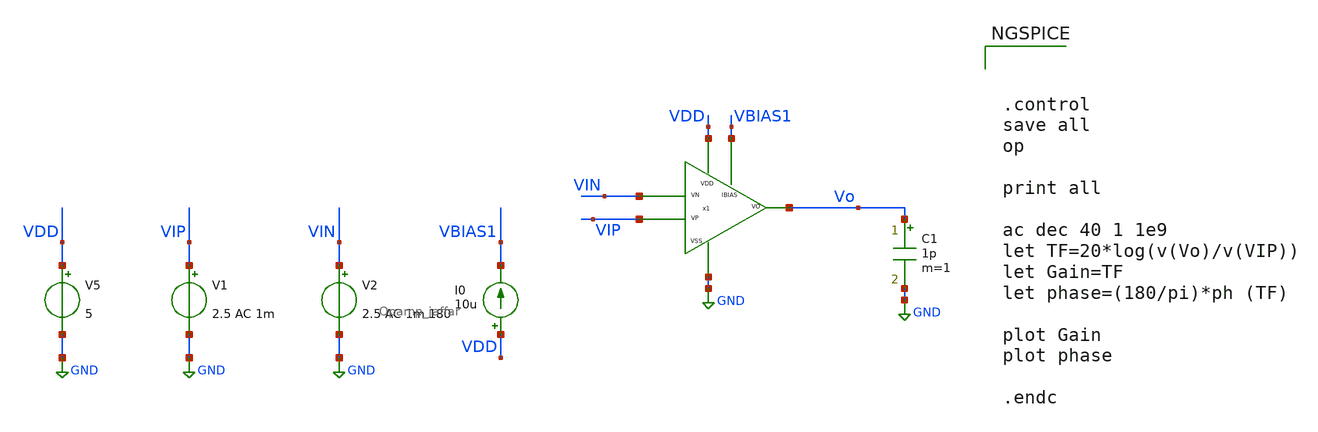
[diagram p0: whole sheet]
** sch_path: xschem/xschem_BGR_Top/Opamp_jaffar_tb_ac.sch
**.subckt Opamp_jaffar_tb_ac
V1 VIP GND 2.5 AC 1m
V2 VIN GND 2.5 AC 1m 180
V5 VDD GND 5
I0 VDD VBIAS1 10u
C1 Vo GND 1p m=1
x1 VDD GND VIP VIN Vo VBIAS1 Opamp_jaffar
**** begin user architecture code



.control
save all
op

print all

ac dec 40 1 1e9
let TF=20*log(v(Vo)/v(VIP))
let Gain=TF
let phase=(180/pi)*ph (TF)

plot Gain
plot phase

.endc


** manual skywater pdks install (with patches applied)
* .lib $::SKYWATER_MODELS/models/sky130.lib.spice tt

** opencircuitdesign pdks install
.lib $::SKYWATER_MODELS/sky130.lib.spice tt


**** end user architecture code
**.ends

* expanding   symbol:  Opamp_jaffar.sym # of pins=6
** sym_path: xschem/xschem_BGR_Top/Opamp_jaffar.sym
** sch_path: xschem/xschem_BGR_Top/Opamp_jaffar.sch
.subckt Opamp_jaffar VDD VSS VP VN VO IBIAS
*.iopin VDD
*.iopin VSS
*.iopin VP
*.iopin VN
*.iopin VO
*.iopin IBIAS
XC1 net7 VO sky130_fd_pr__cap_mim_m3_1 W=24 L=24 MF=1 m=1
XC2 VDD VSS sky130_fd_pr__cap_mim_m3_1 W=30 L=10 MF=1 m=1
XC3 VDD VSS sky130_fd_pr__cap_mim_m3_1 W=30 L=10 MF=1 m=1
XM30 net2 net1 VDD VDD sky130_fd_pr__pfet_g5v0d10v5 L=1 W=5 nf=1 ad='int((nf+1)/2) * W/nf * 0.29' as='int((nf+2)/2) * W/nf * 0.29'
+ pd='2*int((nf+1)/2) * (W/nf + 0.29)' ps='2*int((nf+2)/2) * (W/nf + 0.29)' nrd='0.29 / W' nrs='0.29 / W'
+ sa=0 sb=0 sd=0 mult=1 m=1
XM32 net1 net1 VDD VDD sky130_fd_pr__pfet_g5v0d10v5 L=1 W=5 nf=1 ad='int((nf+1)/2) * W/nf * 0.29' as='int((nf+2)/2) * W/nf * 0.29'
+ pd='2*int((nf+1)/2) * (W/nf + 0.29)' ps='2*int((nf+2)/2) * (W/nf + 0.29)' nrd='0.29 / W' nrs='0.29 / W'
+ sa=0 sb=0 sd=0 mult=1 m=1
XM31 net1 VN net3 VSS sky130_fd_pr__nfet_g5v0d10v5 L=1 W=50 nf=5 ad='int((nf+1)/2) * W/nf * 0.29' as='int((nf+2)/2) * W/nf * 0.29'
+ pd='2*int((nf+1)/2) * (W/nf + 0.29)' ps='2*int((nf+2)/2) * (W/nf + 0.29)' nrd='0.29 / W' nrs='0.29 / W'
+ sa=0 sb=0 sd=0 mult=1 m=1
XM1 net2 VP net3 VSS sky130_fd_pr__nfet_g5v0d10v5 L=1 W=50 nf=5 ad='int((nf+1)/2) * W/nf * 0.29' as='int((nf+2)/2) * W/nf * 0.29'
+ pd='2*int((nf+1)/2) * (W/nf + 0.29)' ps='2*int((nf+2)/2) * (W/nf + 0.29)' nrd='0.29 / W' nrs='0.29 / W'
+ sa=0 sb=0 sd=0 mult=1 m=1
XM2 net3 IBIAS net4 VSS sky130_fd_pr__nfet_g5v0d10v5 L=1 W=50 nf=10 ad='int((nf+1)/2) * W/nf * 0.29'
+ as='int((nf+2)/2) * W/nf * 0.29' pd='2*int((nf+1)/2) * (W/nf + 0.29)' ps='2*int((nf+2)/2) * (W/nf + 0.29)'
+ nrd='0.29 / W' nrs='0.29 / W' sa=0 sb=0 sd=0 mult=1 m=1
XM3 VO IBIAS net6 VSS sky130_fd_pr__nfet_g5v0d10v5 L=1 W=100 nf=20 ad='int((nf+1)/2) * W/nf * 0.29' as='int((nf+2)/2) * W/nf * 0.29'
+ pd='2*int((nf+1)/2) * (W/nf + 0.29)' ps='2*int((nf+2)/2) * (W/nf + 0.29)' nrd='0.29 / W' nrs='0.29 / W'
+ sa=0 sb=0 sd=0 mult=1 m=1
XM4 IBIAS IBIAS net5 VSS sky130_fd_pr__nfet_g5v0d10v5 L=1 W=5 nf=1 ad='int((nf+1)/2) * W/nf * 0.29' as='int((nf+2)/2) * W/nf * 0.29'
+ pd='2*int((nf+1)/2) * (W/nf + 0.29)' ps='2*int((nf+2)/2) * (W/nf + 0.29)' nrd='0.29 / W' nrs='0.29 / W'
+ sa=0 sb=0 sd=0 mult=1 m=1
XM5 net4 net5 VSS VSS sky130_fd_pr__nfet_g5v0d10v5 L=1 W=50 nf=5 ad='int((nf+1)/2) * W/nf * 0.29' as='int((nf+2)/2) * W/nf * 0.29'
+ pd='2*int((nf+1)/2) * (W/nf + 0.29)' ps='2*int((nf+2)/2) * (W/nf + 0.29)' nrd='0.29 / W' nrs='0.29 / W'
+ sa=0 sb=0 sd=0 mult=1 m=1
XM7 net5 net5 VSS VSS sky130_fd_pr__nfet_g5v0d10v5 L=1 W=10 nf=1 ad='int((nf+1)/2) * W/nf * 0.29' as='int((nf+2)/2) * W/nf * 0.29'
+ pd='2*int((nf+1)/2) * (W/nf + 0.29)' ps='2*int((nf+2)/2) * (W/nf + 0.29)' nrd='0.29 / W' nrs='0.29 / W'
+ sa=0 sb=0 sd=0 mult=1 m=1
XM8 net6 net5 VSS VSS sky130_fd_pr__nfet_g5v0d10v5 L=1 W=100 nf=10 ad='int((nf+1)/2) * W/nf * 0.29' as='int((nf+2)/2) * W/nf * 0.29'
+ pd='2*int((nf+1)/2) * (W/nf + 0.29)' ps='2*int((nf+2)/2) * (W/nf + 0.29)' nrd='0.29 / W' nrs='0.29 / W'
+ sa=0 sb=0 sd=0 mult=1 m=1
XM6 VO net2 VDD VDD sky130_fd_pr__pfet_g5v0d10v5 L=1 W=100 nf=10 ad='int((nf+1)/2) * W/nf * 0.29' as='int((nf+2)/2) * W/nf * 0.29'
+ pd='2*int((nf+1)/2) * (W/nf + 0.29)' ps='2*int((nf+2)/2) * (W/nf + 0.29)' nrd='0.29 / W' nrs='0.29 / W'
+ sa=0 sb=0 sd=0 mult=1 m=1
XR1 net7 net2 GND sky130_fd_pr__res_high_po_0p35 L=8 mult=1 m=1
.ends

.GLOBAL GND
.end
